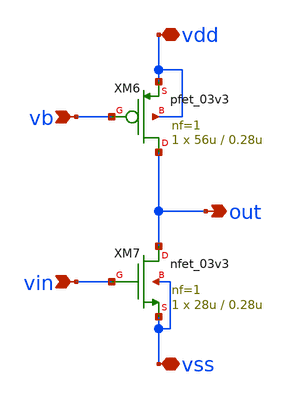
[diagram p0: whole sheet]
** sch_path: opamp/cs.sch
**.subckt cs vb vin out vss vdd
*.ipin vb
*.ipin vin
*.opin out
*.iopin vss
*.iopin vdd
XM6 out vb vdd vdd pfet_03v3 L=0.28u W=56u nf=1 ad='int((nf+1)/2) * W/nf * 0.18u' as='int((nf+2)/2) * W/nf * 0.18u'
+ pd='2*int((nf+1)/2) * (W/nf + 0.18u)' ps='2*int((nf+2)/2) * (W/nf + 0.18u)' nrd='0.18u / W' nrs='0.18u / W'
+ sa=0 sb=0 sd=0 m=1
XM7 out vin vss vss nfet_03v3 L=0.28u W=28u nf=1 ad='int((nf+1)/2) * W/nf * 0.18u' as='int((nf+2)/2) * W/nf * 0.18u'
+ pd='2*int((nf+1)/2) * (W/nf + 0.18u)' ps='2*int((nf+2)/2) * (W/nf + 0.18u)' nrd='0.18u / W' nrs='0.18u / W'
+ sa=0 sb=0 sd=0 m=1
**.ends
.end
